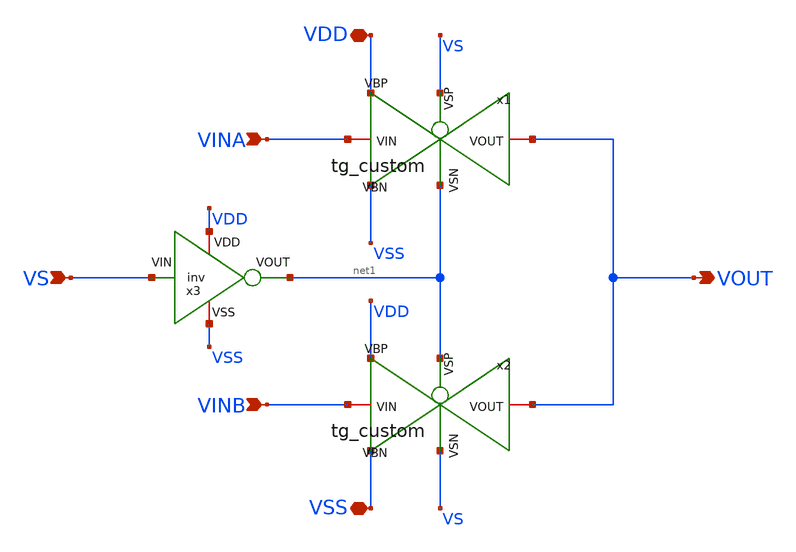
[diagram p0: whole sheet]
** sch_path: Custom_std_cells/MUX_2_1.sch
**.subckt MUX_2_1 VOUT VINA VINB VS VDD VSS
*.opin VOUT
*.ipin VINA
*.ipin VINB
*.ipin VS
*.iopin VDD
*.iopin VSS
x1 VOUT net1 VS VINA VDD VSS tg_custom
x2 VOUT VS net1 VINB VDD VSS tg_custom
x3 VDD net1 VS VSS inv
**.ends

* expanding   symbol:  /foss/designs/PhaseInterpolator/Custom_std_cells/tg_custom.sym # of pins=6
** sym_path: /foss/designs/PhaseInterpolator/Custom_std_cells/tg_custom.sym
** sch_path: /foss/designs/PhaseInterpolator/Custom_std_cells/tg_custom.sch
.subckt tg_custom VOUT VSN VSP VIN VBP VBN
*.iopin VIN
*.iopin VSN
*.iopin VOUT
*.iopin VSP
*.iopin VBN
*.iopin VBP
XM1 VOUT VSN VIN VBN sg13_lv_nmos w=0.15u l=0.13u ng=1 m=1 mm_ok=1
XM2 VOUT VSP VIN VBP sg13_lv_pmos w=0.15u l=0.13u ng=1 m=2 mm_ok=1
.ends

.end
